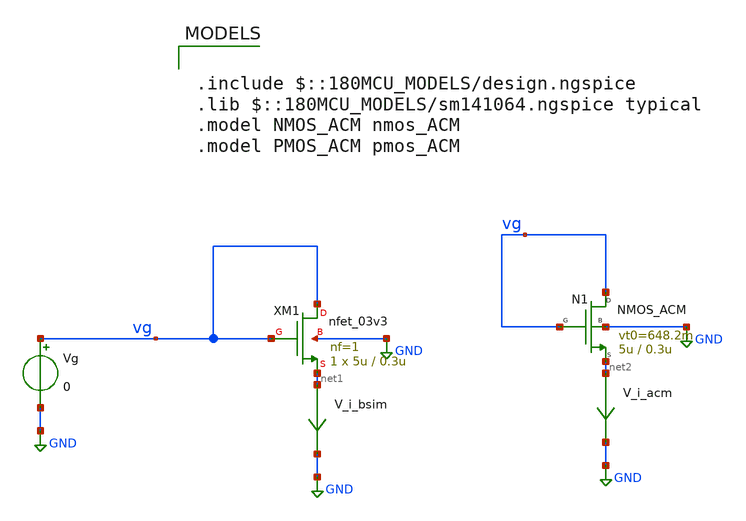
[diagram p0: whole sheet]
** sch_path: gf_tutorials/ACM/Extraction/nmos_zeta_ext.sch
**.subckt nmos_zeta_ext
XM1 vg vg net1 GND nfet_03v3 L=0.3u W=5u nf=1 ad='int((nf+1)/2) * W/nf * 0.18u' as='int((nf+2)/2) * W/nf * 0.18u'
+ pd='2*int((nf+1)/2) * (W/nf + 0.18u)' ps='2*int((nf+2)/2) * (W/nf + 0.18u)' nrd='0.18u / W' nrs='0.18u / W'
+ sa=0 sb=0 sd=0 m=1
N1 vg vg net2 GND NMOS_ACM w=5u l=0.3u n=1.37 is=1.06u vt0=648.2m sigma=26.3m zeta=0.001m
V_i_bsim net1 GND 0
.save i(v_i_bsim)
V_i_acm net2 GND 0
.save i(v_i_acm)
Vg vg GND 0
**** begin user architecture code




.control
  pre_osdi /home/gmaranhao/Desktop/gf180_work/ACM/NMOS_ACM_2V0.osdi
  save all

  dc Vg  0.02 18 1m
  let id_acm = i(V_i_acm)
  let id_bsim = i(V_i_bsim)

  let bsim = deriv(ln(id_acm))/deriv(V(vg))
  let acm = deriv(ln(id_bsim))/deriv(V(vg))

  let bsim_2 = deriv(ln(id_acm))
  let acm_2 = deriv(ln(id_bsim))

  let is = 1.06u
  let if = id_bsim/is
  let zeta_curve = bsim/acm

  save id_acm id_bsim bsim acm if zeta_curve

  write nmos_zeta_ext.raw

.endc




.include $::180MCU_MODELS/design.ngspice
.lib $::180MCU_MODELS/sm141064.ngspice typical
.model NMOS_ACM nmos_ACM
.model PMOS_ACM pmos_ACM

**** end user architecture code
**.ends
.GLOBAL GND
.end
